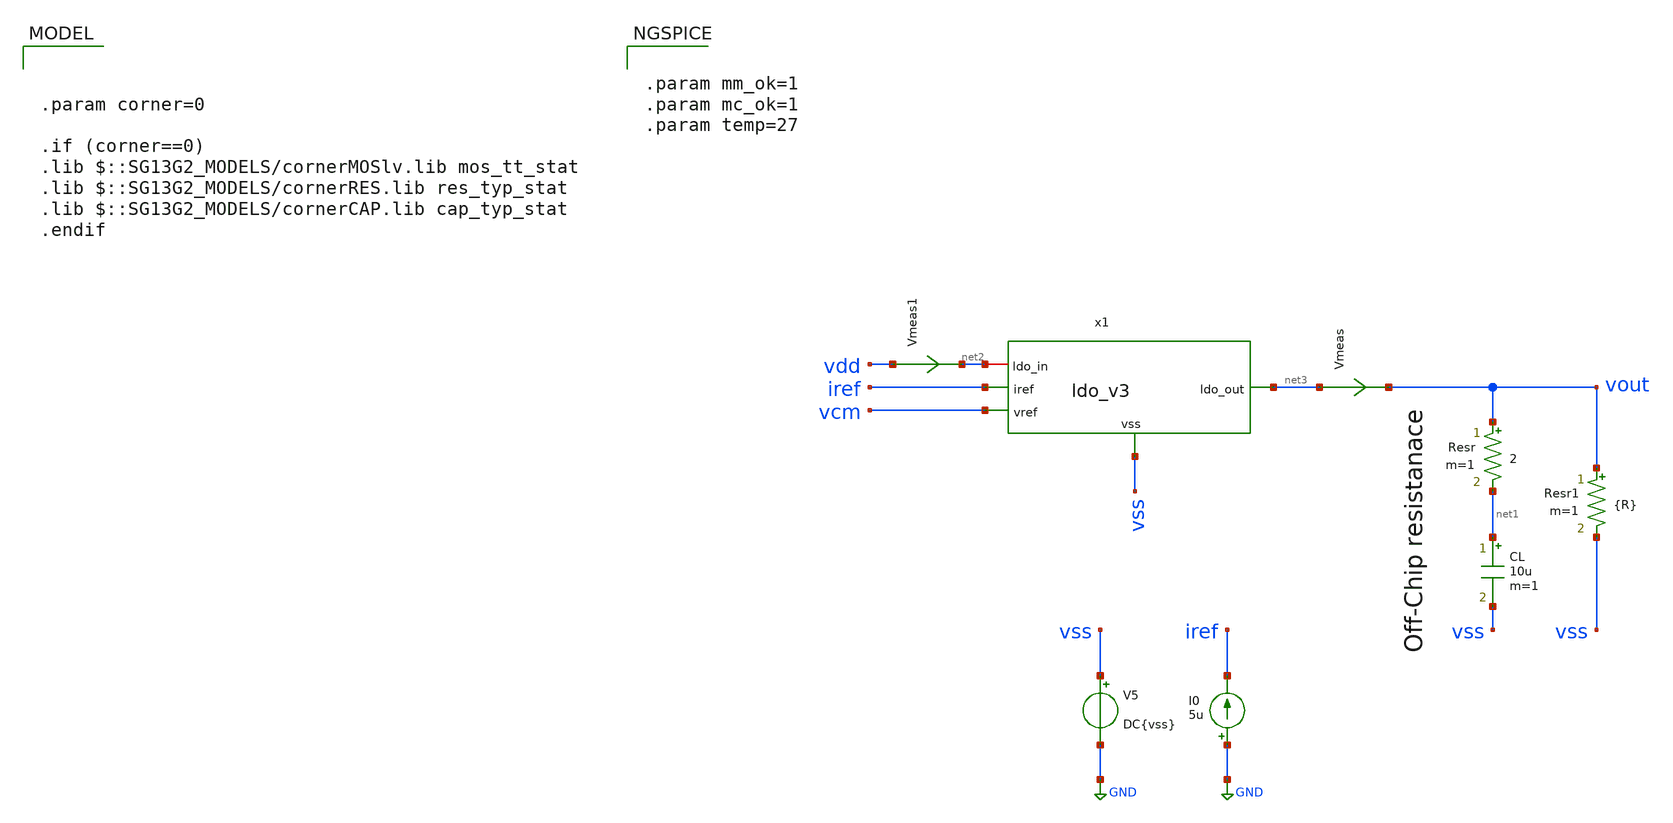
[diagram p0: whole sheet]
** sch_path: AnalogLDO_exampleDesign/val/xschem_simulations/Monte Carlo/mc_ldo_ihp_v3_tb_closeloop.sch
**.subckt mc_ldo_ihp_v3_tb_closeloop
V5 vss GND DC{vss}
Vmeas net3 vout 0
.save i(vmeas)
Vmeas1 vdd net2 0
.save i(vmeas1)
CL net1 vss 10u m=1
Resr vout net1 2 m=1
Resr1 vout vss {R} m=1
I0 GND iref 5u
x1 net2 net3 iref vcm vss ldo_v3
**** begin user architecture code


.param corner=0

.if (corner==0)
.lib $::SG13G2_MODELS/cornerMOSlv.lib mos_tt_stat
.lib $::SG13G2_MODELS/cornerRES.lib res_typ_stat
.lib $::SG13G2_MODELS/cornerCAP.lib cap_typ_stat
.endif




Vs vdd 0 1.8 AC 1
Vref vcm 0 0.9


.param mm_ok=1
.param mc_ok=1
.param temp=27
.save all







.param R=18
*R10 vout 0 {R}
IL vout 0 PWL(0 0.1m 10u 0.1m 20u 10m 30u 10m)
*CL vout 0 50p






.param vdd  = 1.8
.param vss  = 0.0
.param vac  = 60m

.param w857 = 6u
.param l857 = 2u

.param wpar = 15u
.param lpar = 2u
.param mpar = 1

.param w34  = 2u
.param l34  = 1u
.param m34  = 1

.param w6   = 20u
.param l6   = 0.5u
.param m6   = 1

.param w7   = w857*4
.param w5   = w857*1





.param mm_ok=1
.param mc_ok=1
.param temp=27











.control
pre_osdi /home/ac3e/Documents/psp103_nqs.osdi

let mc_runs = 1000
let run = 0
shell rm $HOME_DIR/simulations/csv/mc_ldo_psrr.csv
***************** LOOP *********************
dowhile run < mc_runs
reset
set run=$&run
save all
ac dec 10 10 10G
meas ac vnom_at FIND Vc AT=100k
let v3db = vnom_at*0.707
meas ac freq_3dB when Vc=v3db

meas ac DCG find vdb(vout) at=10

print DCG >> $HOME_DIR/simulations/csv/mc_ldo_psrr.csv
let run=run+1
end
***************** LOOP *********************
.endc






.control
reset

let mc_runs = 1000
let run = 0
shell rm $HOME_DIR/simulations/csv/mc_ldo_line_reg.csv
shell rm $HOME_DIR/simulations/csv/mc_ldo_dropout.csv
***************** LOOP *********************
dowhile run < mc_runs
reset
set run=$&run
dc Vs 0 2.1 0.01

meas dc V_ldo_1.6 FIND v(vout) WHEN v(vdd)=1.6
meas dc V_ldo_2 FIND v(vout) WHEN v(vdd)=2
let line_reg=(V_ldo_1.6-V_ldo_2)/0.4
print line_reg >> $HOME_DIR/simulations/csv/mc_ldo_line_reg.csv

let der = deriv(vout)
meas dc V_ldo_vdropout FIND v(vdd) WHEN der=0.02 CROSS=LAST
let dropout=V_ldo_vdropout-1.2
print dropout >> $HOME_DIR/simulations/csv/mc_ldo_dropout.csv

let run=run+1
end
***************** LOOP *********************
.endc






.control
reset

let mc_runs = 1000
let run = 0
shell rm $HOME_DIR/simulations/csv/mc_ldo_load_reg.csv
***************** LOOP *********************
dowhile run < mc_runs
reset
set run=$&run
alter IL 50u
alter R10 3600k
tran 0.1u 100u

meas TRAN V_ldo_100u FIND v(vout) AT=5u
meas TRAN V_ldo_10m FIND v(vout) AT=100u
let load_reg=V_ldo_100u-V_ldo_10m

print load_reg/9.9 >> $HOME_DIR/simulations/csv/mc_ldo_load_reg.csv



let run=run+1
end
***************** LOOP *********************
.endc



**** end user architecture code
**.ends
.GLOBAL GND
.end
